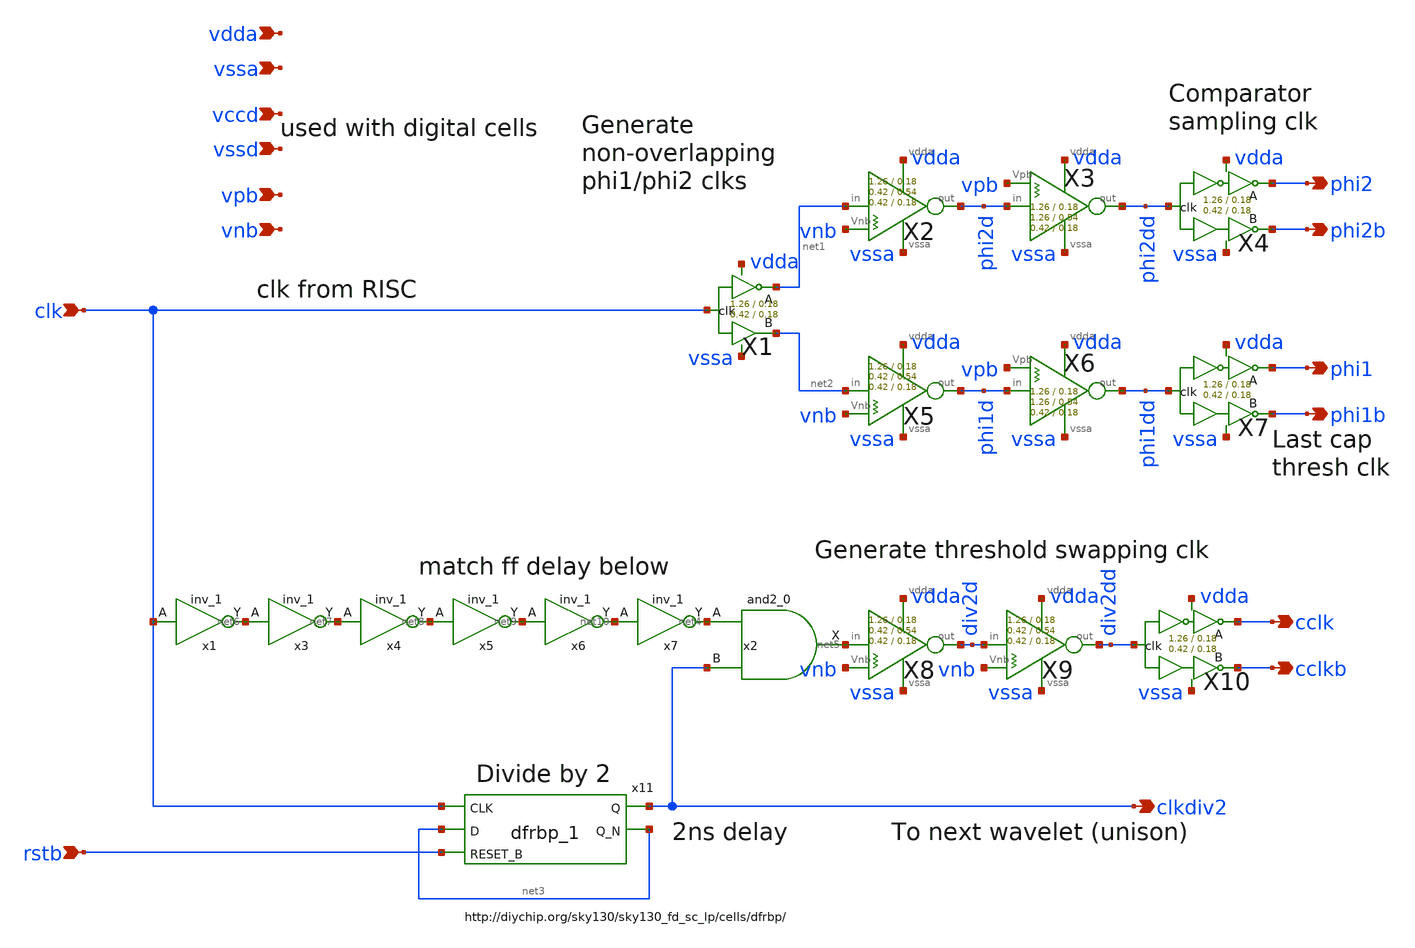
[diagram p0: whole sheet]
** sch_path: xschem/clkgen/filter_clkgen.sch
**.subckt filter_clkgen clk rstb phi2 phi2b phi1 phi1b cclk cclkb clkdiv2 vpb vnb vdda vssa vccd
*+ vssd
*.ipin clk
*.ipin rstb
*.opin phi2
*.opin phi2b
*.opin phi1
*.opin phi1b
*.opin cclk
*.opin cclkb
*.opin clkdiv2
*.ipin vpb
*.ipin vnb
*.ipin vdda
*.ipin vssa
*.ipin vccd
*.ipin vssd
x11 clk net3 rstb vssd vssd vccd vccd clkdiv2 net3 sky130_fd_sc_hd__dfrbp_1
X4 phi2dd phi2 phi2b vdda vssa comp_clks Wpmos=1.26 Lpmos=0.18 Wnmos=0.42 Lnmos=0.18
X7 phi1dd phi1 phi1b vdda vssa comp_clks Wpmos=1.26 Lpmos=0.18 Wnmos=0.42 Lnmos=0.18
X10 div2dd cclk cclkb vdda vssa comp_clks Wpmos=1.26 Lpmos=0.18 Wnmos=0.42 Lnmos=0.18
X1 clk net1 net2 vdda vssa comp_clks_1stage Wpmos=1.26 Lpmos=0.18 Wnmos=0.42 Lnmos=0.18
x2 net4 clkdiv2 vssd vssd vccd vccd net5 sky130_fd_sc_hd__and2_0
X2 net1 phi2d vnb vdda vssa inv_weak_pulldown Wpmos=1.26 Lpmos= Wnmos= Lnmos=0.54
X5 net2 phi1d vnb vdda vssa inv_weak_pulldown Wpmos=1.26 Lpmos= Wnmos= Lnmos=0.54
X8 net5 div2d vnb vdda vssa inv_weak_pulldown Wpmos=1.26 Lpmos= Wnmos= Lnmos=0.54
X9 div2d div2dd vnb vdda vssa inv_weak_pulldown Wpmos=1.26 Lpmos= Wnmos= Lnmos=0.54
X3 phi2d phi2dd vpb vdda vssa inv_weak_pullup Wpmos=1.26 Lpmos=0.54 Wnmos= Lnmos=
X6 phi1d phi1dd vpb vdda vssa inv_weak_pullup Wpmos=1.26 Lpmos=0.54 Wnmos= Lnmos=
x1 clk vssd vssd vccd vccd net6 sky130_fd_sc_hd__inv_1
x3 net6 vssd vssd vccd vccd net7 sky130_fd_sc_hd__inv_1
x4 net7 vssd vssd vccd vccd net8 sky130_fd_sc_hd__inv_1
x5 net8 vssd vssd vccd vccd net9 sky130_fd_sc_hd__inv_1
x6 net9 vssd vssd vccd vccd net10 sky130_fd_sc_hd__inv_1
x7 net10 vssd vssd vccd vccd net4 sky130_fd_sc_hd__inv_1
**.ends
.end
